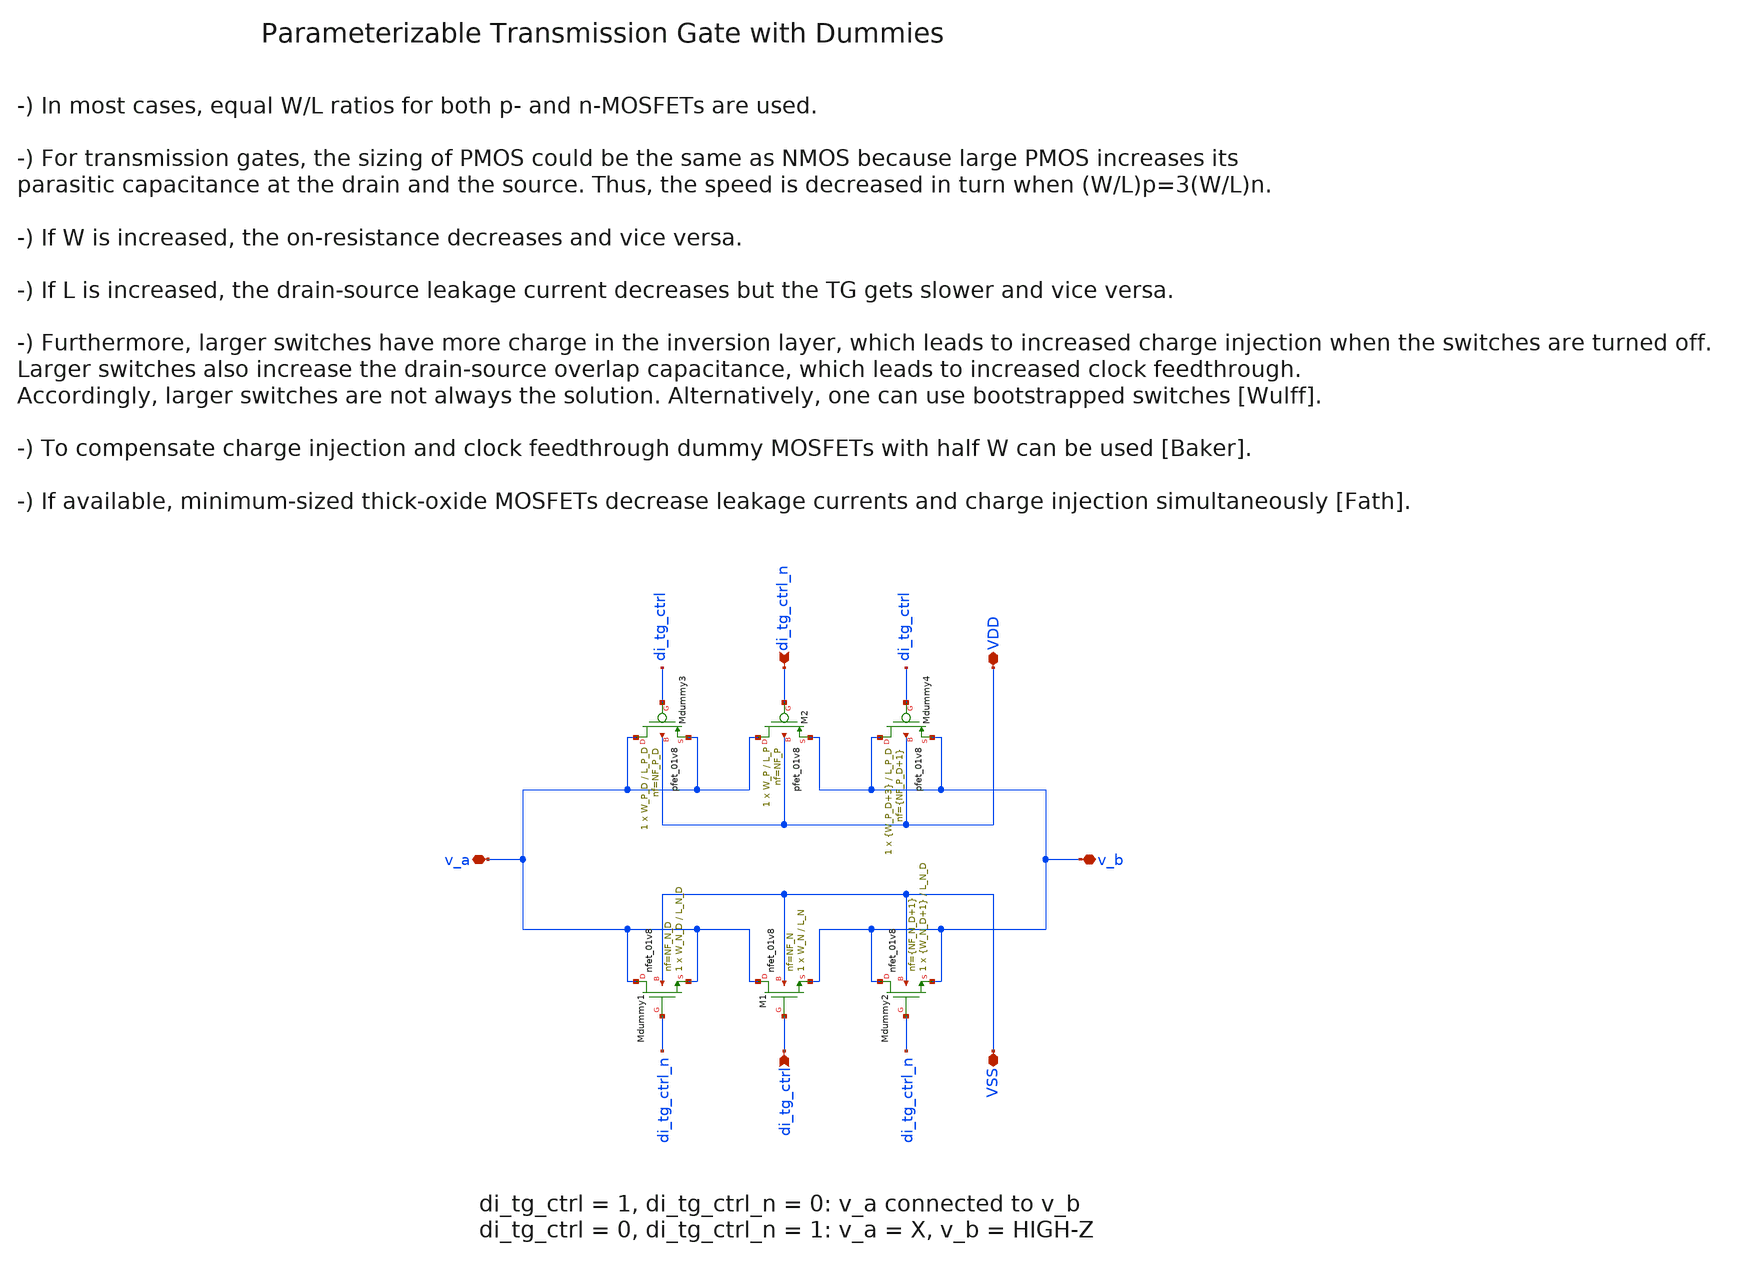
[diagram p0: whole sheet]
** sch_path: sky130/macros/iqmod/schematic/generic/wspr_tx_iqmod_mixer_tg_gen.sch
**.subckt wspr_tx_iqmod_mixer_tg_gen v_a v_b VDD VSS di_tg_ctrl di_tg_ctrl_n
*.iopin v_a
*.iopin v_b
*.iopin VDD
*.iopin VSS
*.ipin di_tg_ctrl
*.ipin di_tg_ctrl_n
XM2 v_a di_tg_ctrl_n v_b VDD sky130_fd_pr__pfet_01v8 L=L_P W=W_P nf=NF_P ad='int((NF_P + 1)/2) * W_P / NF_P * 0.29'
+ as='int((NF_P + 2)/2) * W_P / NF_P * 0.29' pd='2*int((NF_P + 1)/2) * (W_P / NF_P + 0.29)' ps='2*int((NF_P + 2)/2) * (W_P / NF_P + 0.29)'
+ nrd='0.29 / W_P ' nrs='0.29 / W_P ' sa=0 sb=0 sd=0 mult=1 m=1
XMdummy4 v_b di_tg_ctrl v_b VDD sky130_fd_pr__pfet_01v8 L=L_P_D W={W_P_D+3} nf={NF_P_D+1} ad='int(({NF_P_D+1} + 1)/2) * {W_P_D+3} / {NF_P_D+1} * 0.29'
+ as='int(({NF_P_D+1} + 2)/2) * {W_P_D+3} / {NF_P_D+1} * 0.29' pd='2*int(({NF_P_D+1} + 1)/2) * ({W_P_D+3} / {NF_P_D+1} + 0.29)'
+ ps='2*int(({NF_P_D+1} + 2)/2) * ({W_P_D+3} / {NF_P_D+1} + 0.29)' nrd='0.29 / {W_P_D+3} ' nrs='0.29 / {W_P_D+3} '
+ sa=0 sb=0 sd=0 mult=1 m=1
XM1 v_a di_tg_ctrl v_b VSS sky130_fd_pr__nfet_01v8 L=L_N W=W_N nf=NF_N ad='int((NF_N + 1)/2) * W_N / NF_N * 0.29'
+ as='int((NF_N + 2)/2) * W_N / NF_N * 0.29' pd='2*int((NF_N + 1)/2) * (W_N / NF_N + 0.29)' ps='2*int((NF_N + 2)/2) * (W_N / NF_N + 0.29)'
+ nrd='0.29 / W_N ' nrs='0.29 / W_N ' sa=0 sb=0 sd=0 mult=1 m=1
XMdummy2 v_b di_tg_ctrl_n v_b VSS sky130_fd_pr__nfet_01v8 L=L_N_D W={W_N_D+1} nf={NF_N_D+1} ad='int(({NF_N_D+1} + 1)/2) * {W_N_D+1} / {NF_N_D+1} * 0.29'
+ as='int(({NF_N_D+1} + 2)/2) * {W_N_D+1} / {NF_N_D+1} * 0.29' pd='2*int(({NF_N_D+1} + 1)/2) * ({W_N_D+1} / {NF_N_D+1} + 0.29)'
+ ps='2*int(({NF_N_D+1} + 2)/2) * ({W_N_D+1} / {NF_N_D+1} + 0.29)' nrd='0.29 / {W_N_D+1} ' nrs='0.29 / {W_N_D+1} '
+ sa=0 sb=0 sd=0 mult=1 m=1
XMdummy3 v_a di_tg_ctrl v_a VDD sky130_fd_pr__pfet_01v8 L=L_P_D W=W_P_D nf=NF_P_D ad='int((NF_P_D + 1)/2) * W_P_D / NF_P_D * 0.29'
+ as='int((NF_P_D + 2)/2) * W_P_D / NF_P_D * 0.29' pd='2*int((NF_P_D + 1)/2) * (W_P_D / NF_P_D + 0.29)'
+ ps='2*int((NF_P_D + 2)/2) * (W_P_D / NF_P_D + 0.29)' nrd='0.29 / W_P_D ' nrs='0.29 / W_P_D ' sa=0 sb=0
+ sd=0 mult=1 m=1
XMdummy1 v_a di_tg_ctrl_n v_a VSS sky130_fd_pr__nfet_01v8 L=L_N_D W=W_N_D nf=NF_N_D ad='int((NF_N_D + 1)/2) * W_N_D / NF_N_D * 0.29'
+ as='int((NF_N_D + 2)/2) * W_N_D / NF_N_D * 0.29' pd='2*int((NF_N_D + 1)/2) * (W_N_D / NF_N_D + 0.29)'
+ ps='2*int((NF_N_D + 2)/2) * (W_N_D / NF_N_D + 0.29)' nrd='0.29 / W_N_D ' nrs='0.29 / W_N_D ' sa=0 sb=0
+ sd=0 mult=1 m=1
**.ends
.end
